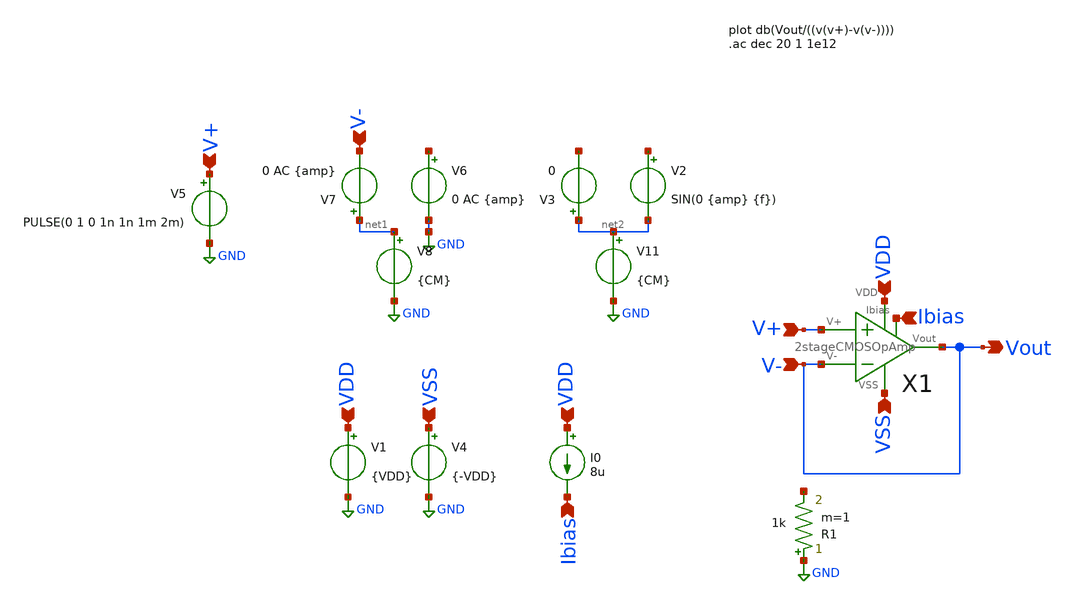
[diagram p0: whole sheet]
** sch_path: ttsky25a-opamp/xschem/2stageCMOSOpAmp_testbed.sch
**.subckt 2stageCMOSOpAmp_testbed VSS VDD V+ VSS VDD V+ Vout V- Ibias VDD Ibias V-
*.ipin VSS
*.ipin VDD
*.ipin V+
*.ipin VSS
*.ipin VDD
*.ipin V+
*.opin Vout
*.ipin V-
*.ipin Ibias
*.ipin VDD
*.ipin Ibias
*.ipin V-
V1 VDD GND {VDD}
V4 VSS GND {-VDD}
V6 net3 GND 0 AC {amp}
V7 net1 V- 0 AC {amp}
V8 net1 GND {CM}
V2 net4 net2 SIN(0 {amp} {f})
V3 net2 net5 0
V11 net2 GND {CM}
X1 V+ Vout VSS VDD Vout Ibias 2stageCMOSOpAmp
I0 VDD Ibias 8u
R1 GND net6 1k m=1
V5 V+ GND PULSE(0 1 0 1n 1n 1m 2m)
**** begin user architecture code



.lib /foss/pdks/sky130A/libs.tech/ngspice/sky130.lib.spice tt
.param CM=0.8 VDD=1.8 amp=1.2 f=500
*.tran 5u 20m
.ac dec 20 1 1e12
.save all

.control
run
*plot vout
plot db(vout/v(v+))
plot 180*cph(vout)/pi
set wr_singlescale
set wr_vecnames
*wrdata /foss/designs/2stageCMOSOpAmp/sim_data/GainvsFreq/gain(max).txt db(vout/v(v+))
*wrdata /foss/designs/2stageCMOSOpAmp/sim_data/sample_waves/a1.3m_f1k_gain700.txt vout
*wrdata /foss/designs/2stageCMOSOpAmp/sim_data/SR/SR.txt vout

.endc


**** end user architecture code
**.ends

* expanding   symbol:  /foss/designs/2stageCMOSOpAmp/ttsky25a-opamp/xschem/2stageCMOSOpAmp.sym # of
*+ pins=6
** sym_path: ttsky25a-opamp/xschem/2stageCMOSOpAmp.sym
** sch_path: ttsky25a-opamp/xschem/2stageCMOSOpAmp.sch
.subckt 2stageCMOSOpAmp V+ V- VSS VDD Vout Ibias
*.ipin VDD
*.ipin VSS
*.opin Vout
*.ipin V+
*.ipin V-
*.ipin Ibias
C1 net2 Vout 0.8p m=1
C2 VSS Vout 2p m=1
XM1 net3 V- net1 VSS sky130_fd_pr__nfet_01v8 L=2.5 W=1 nf=1 ad='int((nf+1)/2) * W/nf * 0.29' as='int((nf+2)/2) * W/nf * 0.29'
+ pd='2*int((nf+1)/2) * (W/nf + 0.29)' ps='2*int((nf+2)/2) * (W/nf + 0.29)' nrd='0.29 / W' nrs='0.29 / W'
+ sa=0 sb=0 sd=0 mult=1 m=1
XM2 net2 V+ net1 VSS sky130_fd_pr__nfet_01v8 L=2.5 W=1 nf=1 ad='int((nf+1)/2) * W/nf * 0.29' as='int((nf+2)/2) * W/nf * 0.29'
+ pd='2*int((nf+1)/2) * (W/nf + 0.29)' ps='2*int((nf+2)/2) * (W/nf + 0.29)' nrd='0.29 / W' nrs='0.29 / W'
+ sa=0 sb=0 sd=0 mult=1 m=1
XM3 net3 net3 VDD VDD sky130_fd_pr__pfet_01v8 L=2.5 W=1 nf=1 ad='int((nf+1)/2) * W/nf * 0.29' as='int((nf+2)/2) * W/nf * 0.29'
+ pd='2*int((nf+1)/2) * (W/nf + 0.29)' ps='2*int((nf+2)/2) * (W/nf + 0.29)' nrd='0.29 / W' nrs='0.29 / W'
+ sa=0 sb=0 sd=0 mult=1 m=1
XM4 net2 net3 VDD VDD sky130_fd_pr__pfet_01v8 L=2.5 W=1 nf=1 ad='int((nf+1)/2) * W/nf * 0.29' as='int((nf+2)/2) * W/nf * 0.29'
+ pd='2*int((nf+1)/2) * (W/nf + 0.29)' ps='2*int((nf+2)/2) * (W/nf + 0.29)' nrd='0.29 / W' nrs='0.29 / W'
+ sa=0 sb=0 sd=0 mult=1 m=1
XM6 Vout net2 VDD VDD sky130_fd_pr__pfet_01v8 L=2.5 W=20 nf=1 ad='int((nf+1)/2) * W/nf * 0.29' as='int((nf+2)/2) * W/nf * 0.29'
+ pd='2*int((nf+1)/2) * (W/nf + 0.29)' ps='2*int((nf+2)/2) * (W/nf + 0.29)' nrd='0.29 / W' nrs='0.29 / W'
+ sa=0 sb=0 sd=0 mult=1 m=1
XM5 net1 Ibias VSS VSS sky130_fd_pr__nfet_01v8 L=2.5 W=0.5 nf=1 ad='int((nf+1)/2) * W/nf * 0.29' as='int((nf+2)/2) * W/nf * 0.29'
+ pd='2*int((nf+1)/2) * (W/nf + 0.29)' ps='2*int((nf+2)/2) * (W/nf + 0.29)' nrd='0.29 / W' nrs='0.29 / W'
+ sa=0 sb=0 sd=0 mult=1 m=1
XM8 Ibias Ibias VSS VSS sky130_fd_pr__nfet_01v8 L=2.5 W=0.5 nf=1 ad='int((nf+1)/2) * W/nf * 0.29' as='int((nf+2)/2) * W/nf * 0.29'
+ pd='2*int((nf+1)/2) * (W/nf + 0.29)' ps='2*int((nf+2)/2) * (W/nf + 0.29)' nrd='0.29 / W' nrs='0.29 / W'
+ sa=0 sb=0 sd=0 mult=1 m=1
XM7 Vout Ibias VSS VSS sky130_fd_pr__nfet_01v8 L=2.5 W=5 nf=1 ad='int((nf+1)/2) * W/nf * 0.29' as='int((nf+2)/2) * W/nf * 0.29'
+ pd='2*int((nf+1)/2) * (W/nf + 0.29)' ps='2*int((nf+2)/2) * (W/nf + 0.29)' nrd='0.29 / W' nrs='0.29 / W'
+ sa=0 sb=0 sd=0 mult=1 m=1
.ends

.GLOBAL GND
.end
